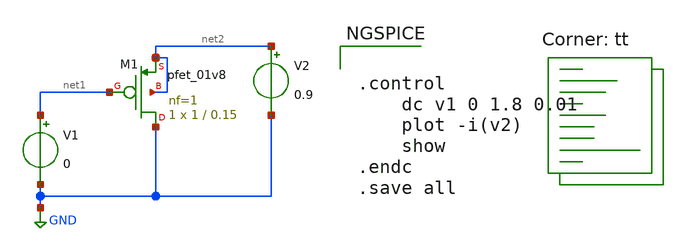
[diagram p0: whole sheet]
** sch_path: cmos_sky130_parameters/pmos_parameters.sch
**.subckt pmos_parameters
V1 net1 GND 0
V2 net2 GND 0.9
XM1 GND net1 net2 net2 sky130_fd_pr__pfet_01v8 L=0.15 W=1 nf=1 ad='int((nf+1)/2) * W/nf * 0.29' as='int((nf+2)/2) * W/nf * 0.29'
+ pd='2*int((nf+1)/2) * (W/nf + 0.29)' ps='2*int((nf+2)/2) * (W/nf + 0.29)' nrd='0.29 / W' nrs='0.29 / W'
+ sa=0 sb=0 sd=0 mult=1 m=1
**** begin user architecture code


.control
	dc v1 0 1.8 0.01
	plot -i(v2)
	show
.endc
.save all


.lib $::SKYWATER_MODELS/sky130.lib.spice tt
**** end user architecture code
**.ends
.GLOBAL GND
.end
